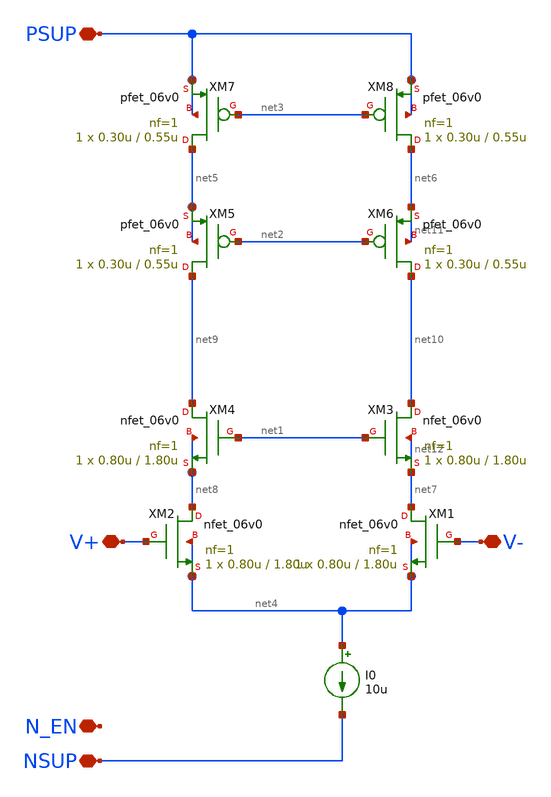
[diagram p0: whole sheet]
** sch_path: xschem/lib/telescopic_nmos_in.sch
**.subckt telescopic_nmos_in NSUP PSUP V+ V- N_EN
*.iopin NSUP
*.iopin PSUP
*.iopin V+
*.iopin V-
*.iopin N_EN
XM1 net7 V- net4 net4 nfet_06v0 L=1.80u W=0.80u nf=1 ad='int((nf+1)/2) * W/nf * 0.18u' as='int((nf+2)/2) * W/nf * 0.18u'
+ pd='2*int((nf+1)/2) * (W/nf + 0.18u)' ps='2*int((nf+2)/2) * (W/nf + 0.18u)' nrd='0.18u / W' nrs='0.18u / W'
+ sa=0 sb=0 sd=0 m=1
XM2 net8 V+ net4 net4 nfet_06v0 L=1.80u W=0.80u nf=1 ad='int((nf+1)/2) * W/nf * 0.18u' as='int((nf+2)/2) * W/nf * 0.18u'
+ pd='2*int((nf+1)/2) * (W/nf + 0.18u)' ps='2*int((nf+2)/2) * (W/nf + 0.18u)' nrd='0.18u / W' nrs='0.18u / W'
+ sa=0 sb=0 sd=0 m=1
XM3 net10 net1 net7 net12 nfet_06v0 L=1.80u W=0.80u nf=1 ad='int((nf+1)/2) * W/nf * 0.18u' as='int((nf+2)/2) * W/nf * 0.18u'
+ pd='2*int((nf+1)/2) * (W/nf + 0.18u)' ps='2*int((nf+2)/2) * (W/nf + 0.18u)' nrd='0.18u / W' nrs='0.18u / W'
+ sa=0 sb=0 sd=0 m=1
XM4 net9 net1 net8 net8 nfet_06v0 L=1.80u W=0.80u nf=1 ad='int((nf+1)/2) * W/nf * 0.18u' as='int((nf+2)/2) * W/nf * 0.18u'
+ pd='2*int((nf+1)/2) * (W/nf + 0.18u)' ps='2*int((nf+2)/2) * (W/nf + 0.18u)' nrd='0.18u / W' nrs='0.18u / W'
+ sa=0 sb=0 sd=0 m=1
XM5 net9 net2 net5 net5 pfet_06v0 L=0.55u W=0.30u nf=1 ad='int((nf+1)/2) * W/nf * 0.18u' as='int((nf+2)/2) * W/nf * 0.18u'
+ pd='2*int((nf+1)/2) * (W/nf + 0.18u)' ps='2*int((nf+2)/2) * (W/nf + 0.18u)' nrd='0.18u / W' nrs='0.18u / W'
+ sa=0 sb=0 sd=0 m=1
XM6 net10 net2 net6 net11 pfet_06v0 L=0.55u W=0.30u nf=1 ad='int((nf+1)/2) * W/nf * 0.18u' as='int((nf+2)/2) * W/nf * 0.18u'
+ pd='2*int((nf+1)/2) * (W/nf + 0.18u)' ps='2*int((nf+2)/2) * (W/nf + 0.18u)' nrd='0.18u / W' nrs='0.18u / W'
+ sa=0 sb=0 sd=0 m=1
XM7 net5 net3 PSUP PSUP pfet_06v0 L=0.55u W=0.30u nf=1 ad='int((nf+1)/2) * W/nf * 0.18u' as='int((nf+2)/2) * W/nf * 0.18u'
+ pd='2*int((nf+1)/2) * (W/nf + 0.18u)' ps='2*int((nf+2)/2) * (W/nf + 0.18u)' nrd='0.18u / W' nrs='0.18u / W'
+ sa=0 sb=0 sd=0 m=1
XM8 net6 net3 PSUP PSUP pfet_06v0 L=0.55u W=0.30u nf=1 ad='int((nf+1)/2) * W/nf * 0.18u' as='int((nf+2)/2) * W/nf * 0.18u'
+ pd='2*int((nf+1)/2) * (W/nf + 0.18u)' ps='2*int((nf+2)/2) * (W/nf + 0.18u)' nrd='0.18u / W' nrs='0.18u / W'
+ sa=0 sb=0 sd=0 m=1
I0 net4 NSUP 10u
**.ends
.end
